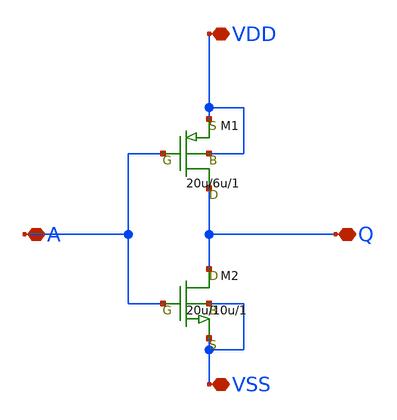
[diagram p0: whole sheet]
** sch_path: Submitted/inverter_Hizuki1030.sch
**.subckt inverter_Hizuki1030 A Q VDD VSS
*.iopin A
*.iopin Q
*.iopin VDD
*.iopin VSS
M1 Q A VDD VDD pch w=20u l=6u as=0 ps=0 ad=0 pd=0 m=1
M2 Q A VSS VSS nch w=20u l=10u as=0 ps=0 ad=0 pd=0 m=1
**.ends
.end
